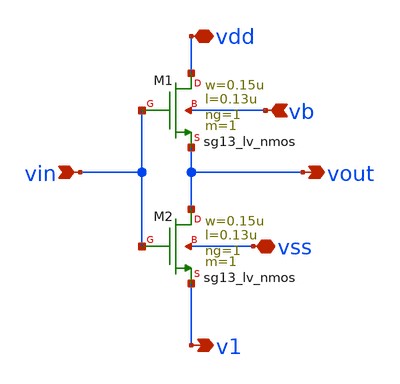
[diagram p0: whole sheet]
** sch_path: xschem/test.sch
**.subckt test vin vout vdd vb vss v1
*.ipin vin
*.opin vout
*.iopin vdd
*.ipin vb
*.iopin vss
*.opin v1
XM1 vdd vin vout vb sg13_lv_nmos w=0.15u l=0.13u ng=1 m=1 mm_ok=1
XM2 vout vin v1 vss sg13_lv_nmos w=0.15u l=0.13u ng=1 m=1 mm_ok=1
**.ends
.end
